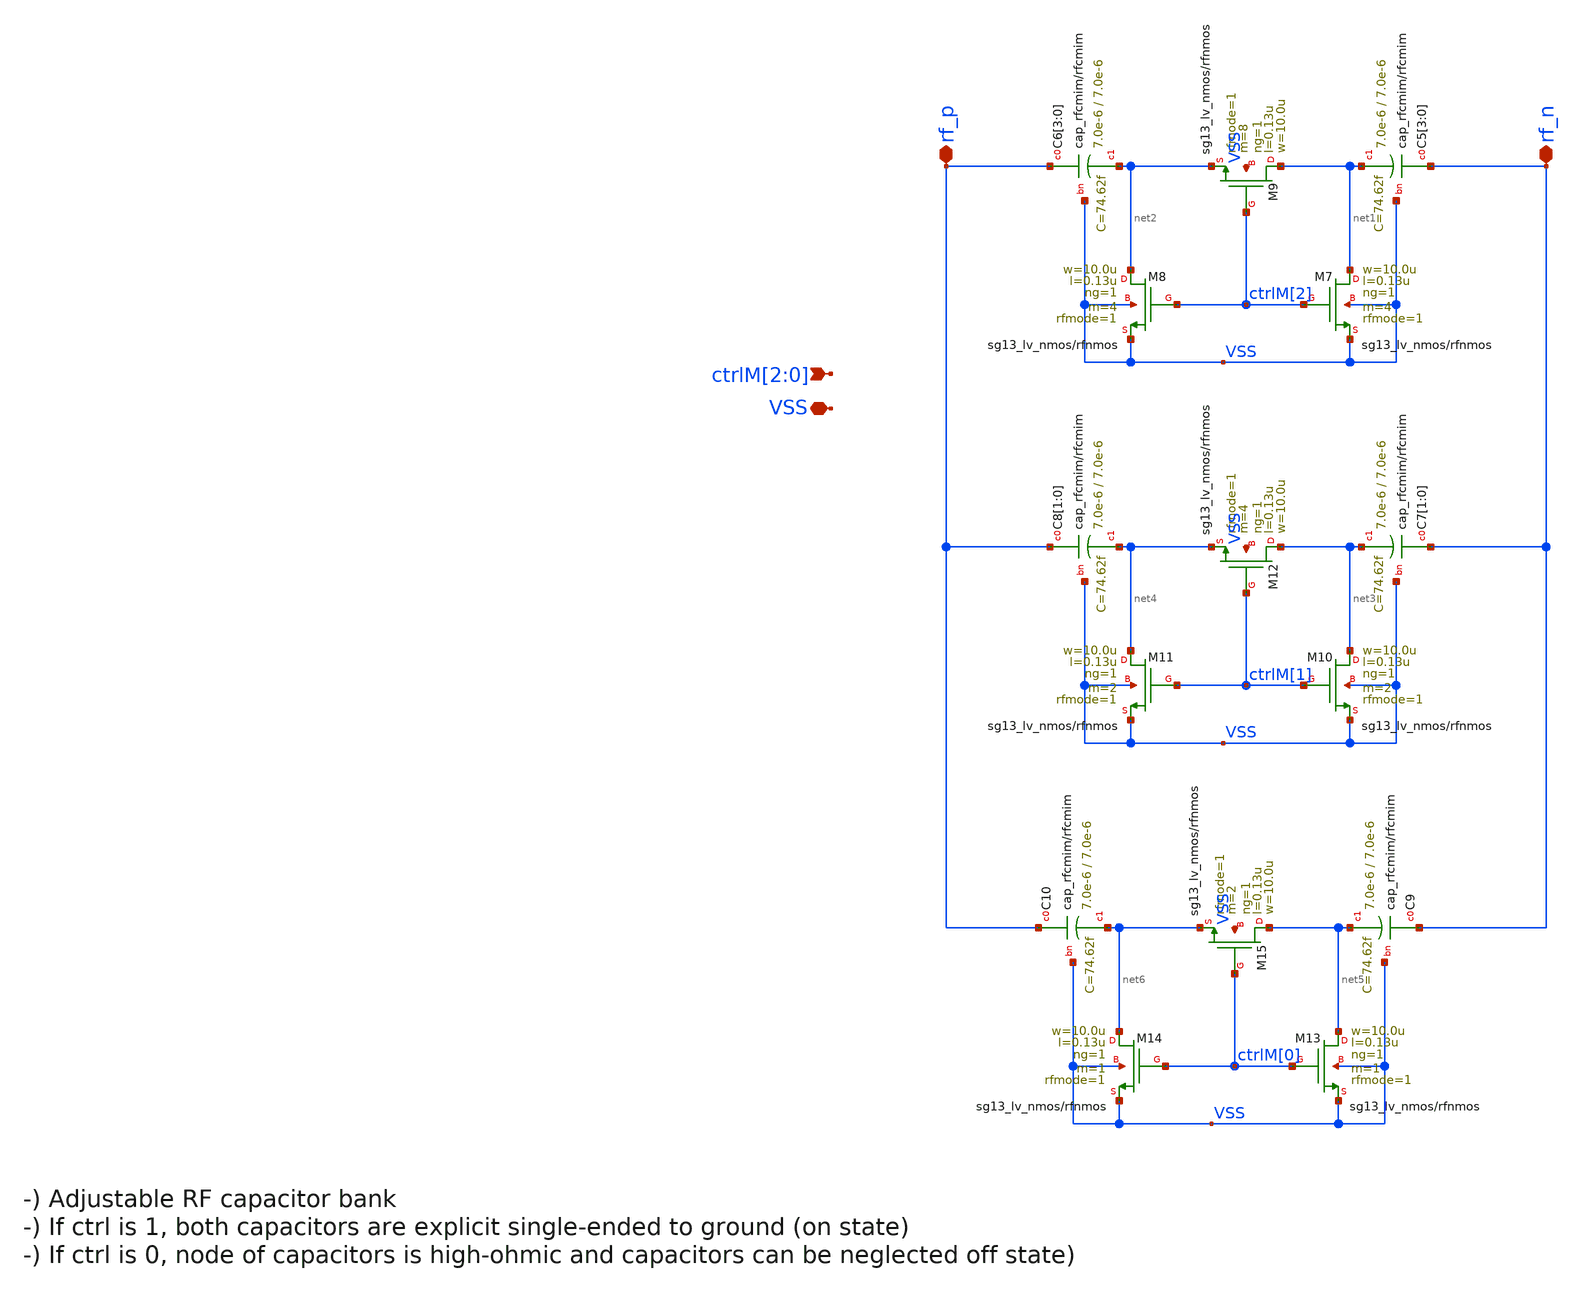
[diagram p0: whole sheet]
** sch_path: xschem/iruwbtx7_PA_capBank.sch
**.subckt iruwbtx7_PA_capBank ctrlM[2],ctrlM[1],ctrlM[0] VSS rf_p rf_n
*.ipin ctrlM[2],ctrlM[1],ctrlM[0]
*.iopin VSS
*.iopin rf_p
*.iopin rf_n
XC5[3] rf_n net1 VSS cap_rfcmim w=7.0e-6 l=7.0e-6 wfeed=1.0e-6 m=1 mm_ok=1
XC5[2] rf_n net1 VSS cap_rfcmim w=7.0e-6 l=7.0e-6 wfeed=1.0e-6 m=1 mm_ok=1
XC5[1] rf_n net1 VSS cap_rfcmim w=7.0e-6 l=7.0e-6 wfeed=1.0e-6 m=1 mm_ok=1
XC5[0] rf_n net1 VSS cap_rfcmim w=7.0e-6 l=7.0e-6 wfeed=1.0e-6 m=1 mm_ok=1
XM7 net1 ctrlM[2] VSS VSS sg13_lv_nmos w=10.0u l=0.13u ng=1 m=4 rfmode=1 mm_ok=1
XM8 net2 ctrlM[2] VSS VSS sg13_lv_nmos w=10.0u l=0.13u ng=1 m=4 rfmode=1 mm_ok=1
XM9 net1 ctrlM[2] net2 VSS sg13_lv_nmos w=10.0u l=0.13u ng=1 m=8 rfmode=1 mm_ok=1
XC6[3] rf_p net2 VSS cap_rfcmim w=7.0e-6 l=7.0e-6 wfeed=1.0e-6 m=1 mm_ok=1
XC6[2] rf_p net2 VSS cap_rfcmim w=7.0e-6 l=7.0e-6 wfeed=1.0e-6 m=1 mm_ok=1
XC6[1] rf_p net2 VSS cap_rfcmim w=7.0e-6 l=7.0e-6 wfeed=1.0e-6 m=1 mm_ok=1
XC6[0] rf_p net2 VSS cap_rfcmim w=7.0e-6 l=7.0e-6 wfeed=1.0e-6 m=1 mm_ok=1
XC7[1] rf_n net3 VSS cap_rfcmim w=7.0e-6 l=7.0e-6 wfeed=1.0e-6 m=1 mm_ok=1
XC7[0] rf_n net3 VSS cap_rfcmim w=7.0e-6 l=7.0e-6 wfeed=1.0e-6 m=1 mm_ok=1
XM10 net3 ctrlM[1] VSS VSS sg13_lv_nmos w=10.0u l=0.13u ng=1 m=2 rfmode=1 mm_ok=1
XM11 net4 ctrlM[1] VSS VSS sg13_lv_nmos w=10.0u l=0.13u ng=1 m=2 rfmode=1 mm_ok=1
XM12 net3 ctrlM[1] net4 VSS sg13_lv_nmos w=10.0u l=0.13u ng=1 m=4 rfmode=1 mm_ok=1
XC8[1] rf_p net4 VSS cap_rfcmim w=7.0e-6 l=7.0e-6 wfeed=1.0e-6 m=1 mm_ok=1
XC8[0] rf_p net4 VSS cap_rfcmim w=7.0e-6 l=7.0e-6 wfeed=1.0e-6 m=1 mm_ok=1
XC9 rf_n net5 VSS cap_rfcmim w=7.0e-6 l=7.0e-6 wfeed=1.0e-6 m=1 mm_ok=1
XM13 net5 ctrlM[0] VSS VSS sg13_lv_nmos w=10.0u l=0.13u ng=1 m=1 rfmode=1 mm_ok=1
XM14 net6 ctrlM[0] VSS VSS sg13_lv_nmos w=10.0u l=0.13u ng=1 m=1 rfmode=1 mm_ok=1
XM15 net5 ctrlM[0] net6 VSS sg13_lv_nmos w=10.0u l=0.13u ng=1 m=2 rfmode=1 mm_ok=1
XC10 rf_p net6 VSS cap_rfcmim w=7.0e-6 l=7.0e-6 wfeed=1.0e-6 m=1 mm_ok=1
**.ends
.end
